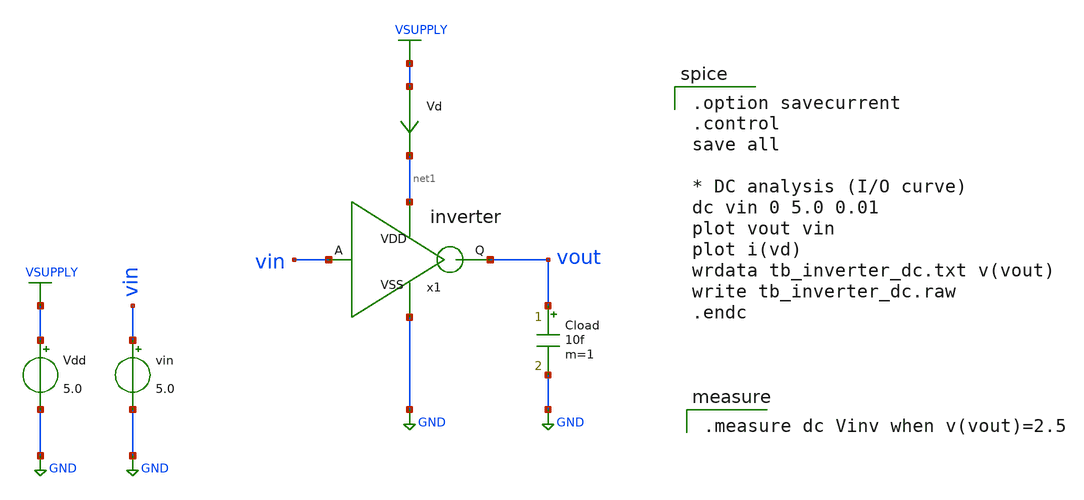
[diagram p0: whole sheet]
** sch_path: member_project/AM_Radio/Yamada3/xschem/tb_inverter_dc.sch
**.subckt tb_inverter_dc
Vdd VSUPPLY GND 5.0
vin vin GND 5.0
Cload vout GND 10f m=1
Vd VSUPPLY net1 0
.save i(vd)
x1 net1 vin vout GND inverter
**** begin user architecture code

.option savecurrent
.control
save all

* DC analysis (I/O curve)
dc vin 0 5.0 0.01
plot vout vin
plot i(vd)
wrdata tb_inverter_dc.txt v(vout)
write tb_inverter_dc.raw
.endc


.measure dc Vinv when v(vout)=2.5

 .include $::LIB/ip62_models
**** end user architecture code
**.ends

* expanding   symbol:  inverter.sym # of pins=4
** sym_path: member_project/AM_Radio/Yamada3/xschem/inverter.sym
** sch_path: member_project/AM_Radio/Yamada3/xschem/inverter.sch
.subckt inverter VDD A Q VSS
*.iopin VDD
*.iopin VSS
*.ipin A
*.opin Q
XM1 Q A VDD VDD PMOS w=30u l=5u as=0 ad=0 ps=0 pd=0 nrd=0 nrs=0 m=1
XM2 Q A VSS VSS NMOS w=10u l=5u as=0 ad=0 ps=0 pd=0 nrd=0 nrs=0 m=1
.ends

.GLOBAL VSUPPLY
.GLOBAL GND
.end
